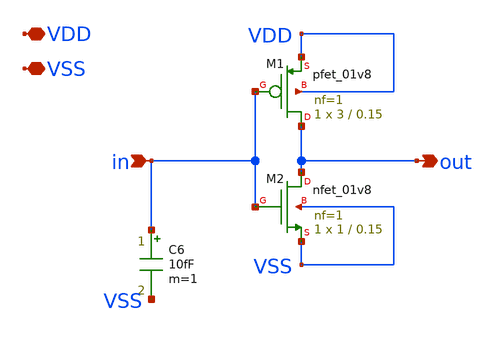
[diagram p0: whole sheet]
** sch_path: xschem/inverter.sch
**.subckt inverter out VDD VSS in
*.opin out
*.iopin VDD
*.iopin VSS
*.ipin in
XM1 out in VDD VDD sky130_fd_pr__pfet_01v8 L=0.15 W=3 nf=1 ad='int((nf+1)/2) * W/nf * 0.29' as='int((nf+2)/2) * W/nf * 0.29'
+ pd='2*int((nf+1)/2) * (W/nf + 0.29)' ps='2*int((nf+2)/2) * (W/nf + 0.29)' nrd='0.29 / W' nrs='0.29 / W'
+ sa=0 sb=0 sd=0 mult=1 m=1
XM2 out in VSS VSS sky130_fd_pr__nfet_01v8 L=0.15 W=1 nf=1 ad='int((nf+1)/2) * W/nf * 0.29' as='int((nf+2)/2) * W/nf * 0.29'
+ pd='2*int((nf+1)/2) * (W/nf + 0.29)' ps='2*int((nf+2)/2) * (W/nf + 0.29)' nrd='0.29 / W' nrs='0.29 / W'
+ sa=0 sb=0 sd=0 mult=1 m=1
C6 in VSS 10fF m=1
**.ends
.end
